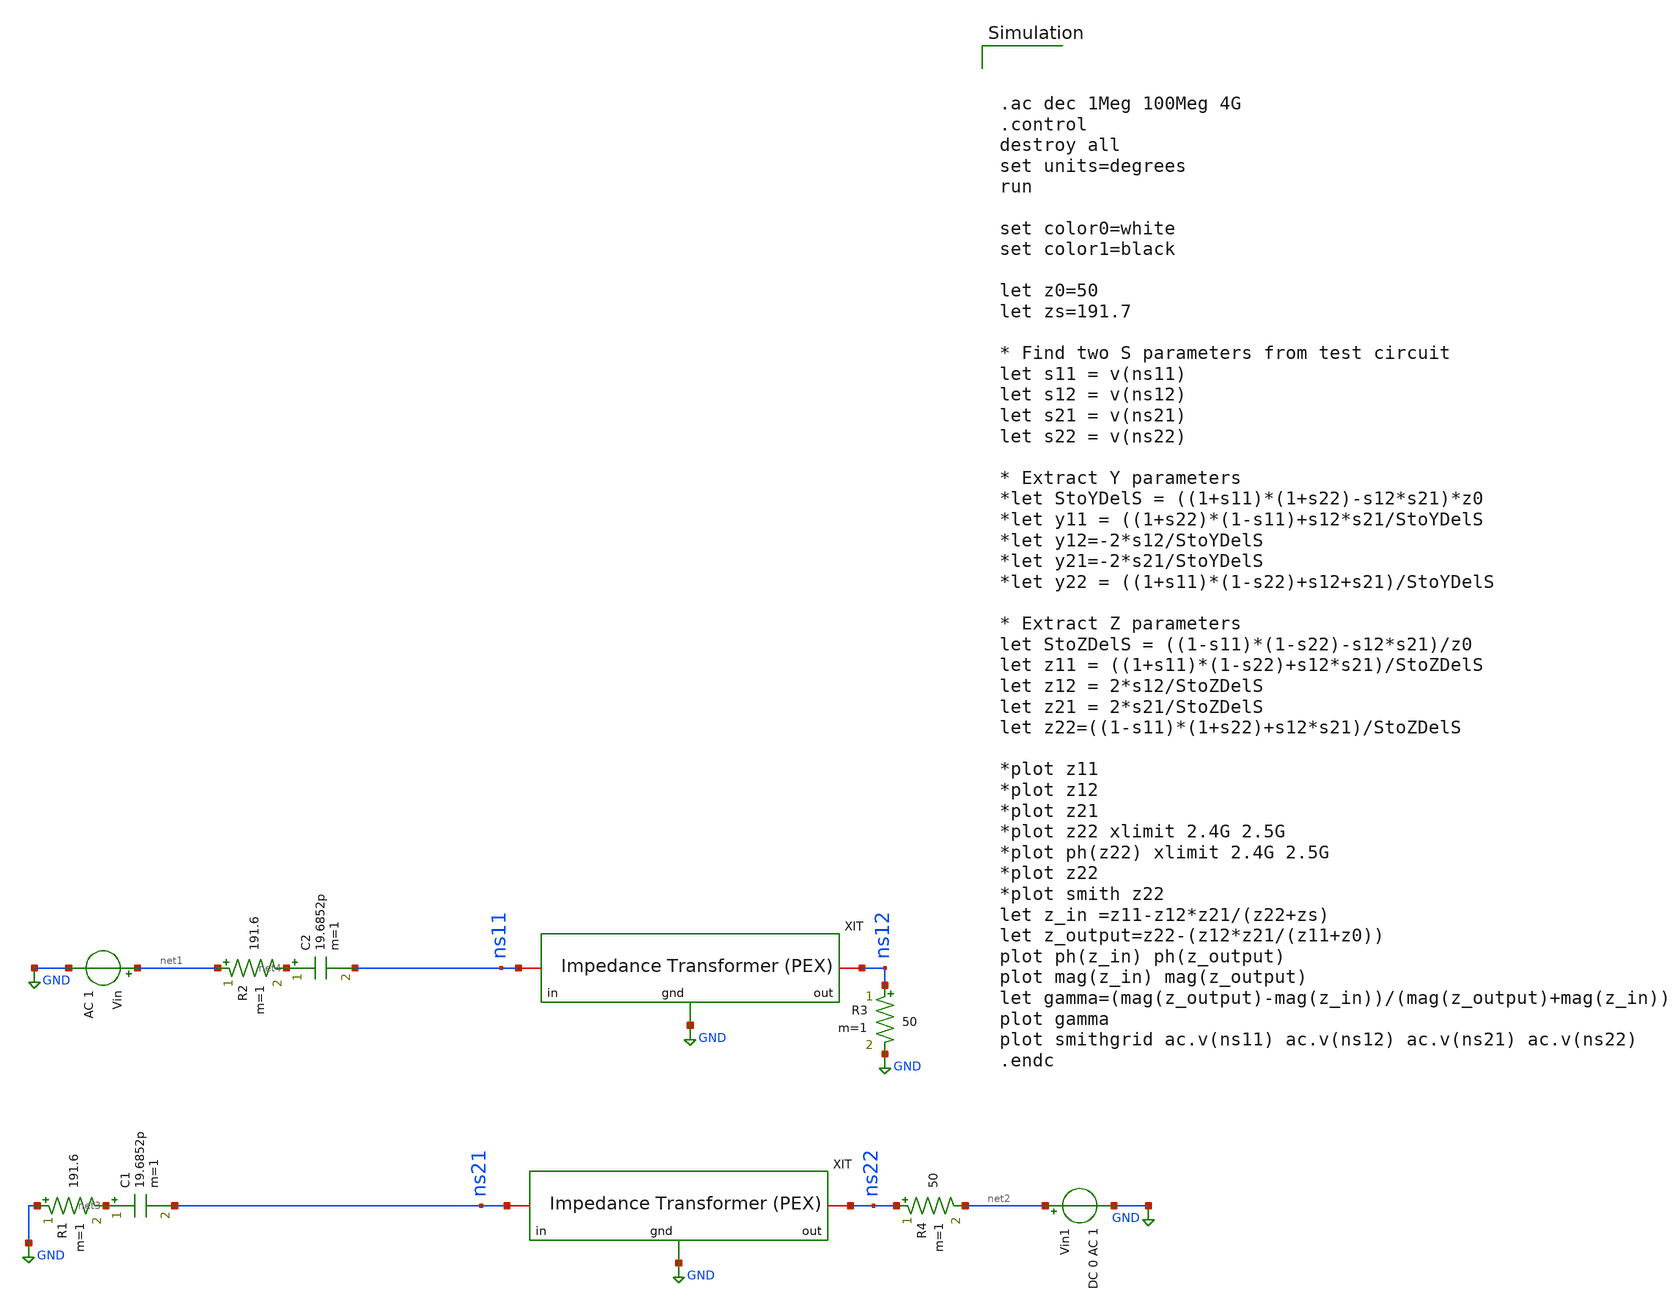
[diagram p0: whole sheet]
** sch_path: impedance-transformer/xschem/impedance-transformer-pex_tb-ac.sch
**.subckt impedance-transformer-pex_tb-ac
Vin net1 GND AC 1
Vin1 net2 GND DC 0 AC 1
R3 ns12 GND 50 m=1
R4 ns22 net2 50 m=1
x1 ns11 ns12 GND impedance-transformer-pex
x2 ns21 ns22 GND impedance-transformer-pex
R1 GND net3 191.6 m=1
C1 net3 ns21 19.6852p m=1
R2 net1 net4 191.6 m=1
C2 net4 ns11 19.6852p m=1
**** begin user architecture code



.ac dec 1Meg 100Meg 4G
.control
destroy all
set units=degrees
run

set color0=white
set color1=black

let z0=50
let zs=191.7

* Find two S parameters from test circuit
let s11 = v(ns11)
let s12 = v(ns12)
let s21 = v(ns21)
let s22 = v(ns22)

* Extract Y parameters
*let StoYDelS = ((1+s11)*(1+s22)-s12*s21)*z0
*let y11 = ((1+s22)*(1-s11)+s12*s21/StoYDelS
*let y12=-2*s12/StoYDelS
*let y21=-2*s21/StoYDelS
*let y22 = ((1+s11)*(1-s22)+s12+s21)/StoYDelS

* Extract Z parameters
let StoZDelS = ((1-s11)*(1-s22)-s12*s21)/z0
let z11 = ((1+s11)*(1-s22)+s12*s21)/StoZDelS
let z12 = 2*s12/StoZDelS
let z21 = 2*s21/StoZDelS
let z22=((1-s11)*(1+s22)+s12*s21)/StoZDelS

*plot z11
*plot z12
*plot z21
*plot z22 xlimit 2.4G 2.5G
*plot ph(z22) xlimit 2.4G 2.5G
*plot z22
*plot smith z22
let z_in =z11-z12*z21/(z22+zs)
let z_output=z22-(z12*z21/(z11+z0))
plot ph(z_in) ph(z_output)
plot mag(z_in) mag(z_output)
let gamma=(mag(z_output)-mag(z_in))/(mag(z_output)+mag(z_in))
plot gamma
plot smithgrid ac.v(ns11) ac.v(ns12) ac.v(ns21) ac.v(ns22)
.endc


.lib /home/hugodg/sky130_workspace/skywater-pdk/libraries/sky130_fd_pr_ngspice/latest/models/sky130.lib.spice tt

**** end user architecture code
**.ends

* expanding   symbol:
*+  /home/hugodg/projects-sky130/temp-sensor/impedance-transformer/xschem/impedance-transformer-pex.sym # of pins=3
** sym_path: impedance-transformer/xschem/impedance-transformer-pex.sym
** sch_path: impedance-transformer/xschem/impedance-transformer-pex.sch
.subckt impedance-transformer-pex in out gnd
*.iopin gnd
*.iopin in
*.iopin out
**** begin user architecture code

* NGSPICE file created from impedance-transformer.ext - technology: sky130A

.subckt sky130_fd_pr__cap_mim_m3_2_4GE4YE c2_n2372_n7179# m4_n2472_n7279# VSUBS
X0 c2_n2372_n7179# m4_n2472_n7279# sky130_fd_pr__cap_mim_m3_2 l=2.293e+07u w=2.293e+07u
X1 c2_n2372_n7179# m4_n2472_n7279# sky130_fd_pr__cap_mim_m3_2 l=2.293e+07u w=2.293e+07u
X2 c2_n2372_n7179# m4_n2472_n7279# sky130_fd_pr__cap_mim_m3_2 l=2.293e+07u w=2.293e+07u
C0 m4_n2472_n7279# c2_n2372_n7179# 105.86fF
C1 c2_n2372_n7179# VSUBS 0.26fF
C2 m4_n2472_n7279# VSUBS 28.10fF
.ends

.subckt sky130_fd_pr__cap_mim_m3_2_8BWDGQ c2_n2486_n10078# m4_n2586_n10178# VSUBS
X0 c2_n2486_n10078# m4_n2586_n10178# sky130_fd_pr__cap_mim_m3_2 l=2.407e+07u w=2.407e+07u
X1 c2_n2486_n10078# m4_n2586_n10178# sky130_fd_pr__cap_mim_m3_2 l=2.407e+07u w=2.407e+07u
X2 c2_n2486_n10078# m4_n2586_n10178# sky130_fd_pr__cap_mim_m3_2 l=2.407e+07u w=2.407e+07u
X3 c2_n2486_n10078# m4_n2586_n10178# sky130_fd_pr__cap_mim_m3_2 l=2.407e+07u w=2.407e+07u
C0 m4_n2586_n10178# c2_n2486_n10078# 154.16fF
C1 c2_n2486_n10078# VSUBS 0.30fF
C2 m4_n2586_n10178# VSUBS 40.10fF
.ends

*.subckt impedance-transformer gnd out in
Xsky130_fd_pr__cap_mim_m3_2_4GE4YE_1 in gnd gnd sky130_fd_pr__cap_mim_m3_2_4GE4YE
Xsky130_fd_pr__cap_mim_m3_2_4GE4YE_2 in gnd gnd sky130_fd_pr__cap_mim_m3_2_4GE4YE
Xsky130_fd_pr__cap_mim_m3_2_8BWDGQ_0 out gnd gnd sky130_fd_pr__cap_mim_m3_2_8BWDGQ
Xsky130_fd_pr__cap_mim_m3_2_8BWDGQ_1 out gnd gnd sky130_fd_pr__cap_mim_m3_2_8BWDGQ
Xsky130_fd_pr__cap_mim_m3_2_8BWDGQ_2 out gnd gnd sky130_fd_pr__cap_mim_m3_2_8BWDGQ
Xsky130_fd_pr__cap_mim_m3_2_8BWDGQ_3 out gnd gnd sky130_fd_pr__cap_mim_m3_2_8BWDGQ
Xsky130_fd_pr__cap_mim_m3_2_4GE4YE_0 in gnd gnd sky130_fd_pr__cap_mim_m3_2_4GE4YE

R0 in in.n1 0.704
R1 in.n0 in.t3 0.125
R2 in.n1 in.n0 0.089
R3 in.t8 in.t7 0.066
R4 in.t6 in.t8 0.066
R5 in.t2 in.t1 0.066
R6 in.t0 in.t2 0.066
R7 in.t5 in.t4 0.066
R8 in.t3 in.t5 0.066
R9 in.n1 in.t6 0.037
R10 in.n0 in.t0 0.037
R11 out out.n2 0.325
R12 out.n0 out.t13 0.094
R13 out.n1 out.n0 0.079
R14 out.t14 out.t15 0.066
R15 out.t12 out.t14 0.066
R16 out.t13 out.t12 0.066
R17 out.t10 out.t11 0.066
R18 out.t8 out.t10 0.066
R19 out.t9 out.t8 0.066
R20 out.t6 out.t7 0.066
R21 out.t4 out.t6 0.066
R22 out.t5 out.t4 0.066
R23 out.t2 out.t3 0.066
R24 out.t0 out.t2 0.066
R25 out.t1 out.t0 0.066
R26 out.n2 out.n1 0.064
R27 out.n2 out.t1 0.041
R28 out.n0 out.t9 0.018
R29 out.n1 out.t5 0.018
C0 out.t7 gnd 33.56fF
C1 out.t6 gnd 33.64fF
C2 out.t4 gnd 33.64fF
C3 out.t5 gnd 29.89fF
C4 out.t11 gnd 33.56fF
C5 out.t10 gnd 33.64fF
C6 out.t8 gnd 33.64fF
C7 out.t9 gnd 29.89fF
C8 out.t15 gnd 33.56fF
C9 out.t14 gnd 33.64fF
C10 out.t12 gnd 33.64fF
C11 out.t13 gnd 89.97fF
C12 out.n0 gnd 28.18fF $ **FLOATING
C13 out.n1 gnd 13.26fF $ **FLOATING
C14 out.t3 gnd 33.56fF
C15 out.t2 gnd 33.64fF
C16 out.t0 gnd 33.64fF
C17 out.t1 gnd 33.03fF
C18 out.n2 gnd 41.48fF $ **FLOATING
C19 in.t7 gnd 32.16fF
C20 in.t8 gnd 32.25fF
C21 in.t6 gnd 30.87fF
C22 in.t1 gnd 32.16fF
C23 in.t2 gnd 32.25fF
C24 in.t0 gnd 30.87fF
C25 in.t4 gnd 32.16fF
C26 in.t5 gnd 32.25fF
C27 in.t3 gnd 30.02fF
C28 in.n0 gnd 11.26fF $ **FLOATING
C29 in.n1 gnd 57.09fF $ **FLOATING
C30 in gnd 55.98fF
C31 out gnd 70.58fF
*.ends



**** end user architecture code
x1 in out l1
.ends


* expanding   symbol:  /home/hugodg/projects-sky130/temp-sensor/impedance-transformer/xschem/l1.sym
*+ # of pins=2
** sym_path: impedance-transformer/xschem/l1.sym
** sch_path: impedance-transformer/xschem/l1.sch
.subckt l1 p1 p2
*.iopin p2
*.iopin p1
L0 p1 net3 598p m=1
Cs1 p1 net1 26.59f m=1
Cs2 p2 net2 25.14f m=1
Rs1 net1 GND 63.55 m=1
Rs2 net2 GND 19.11 m=1
R1 p2 net3 2.89 m=1
.ends

.GLOBAL GND
.end
